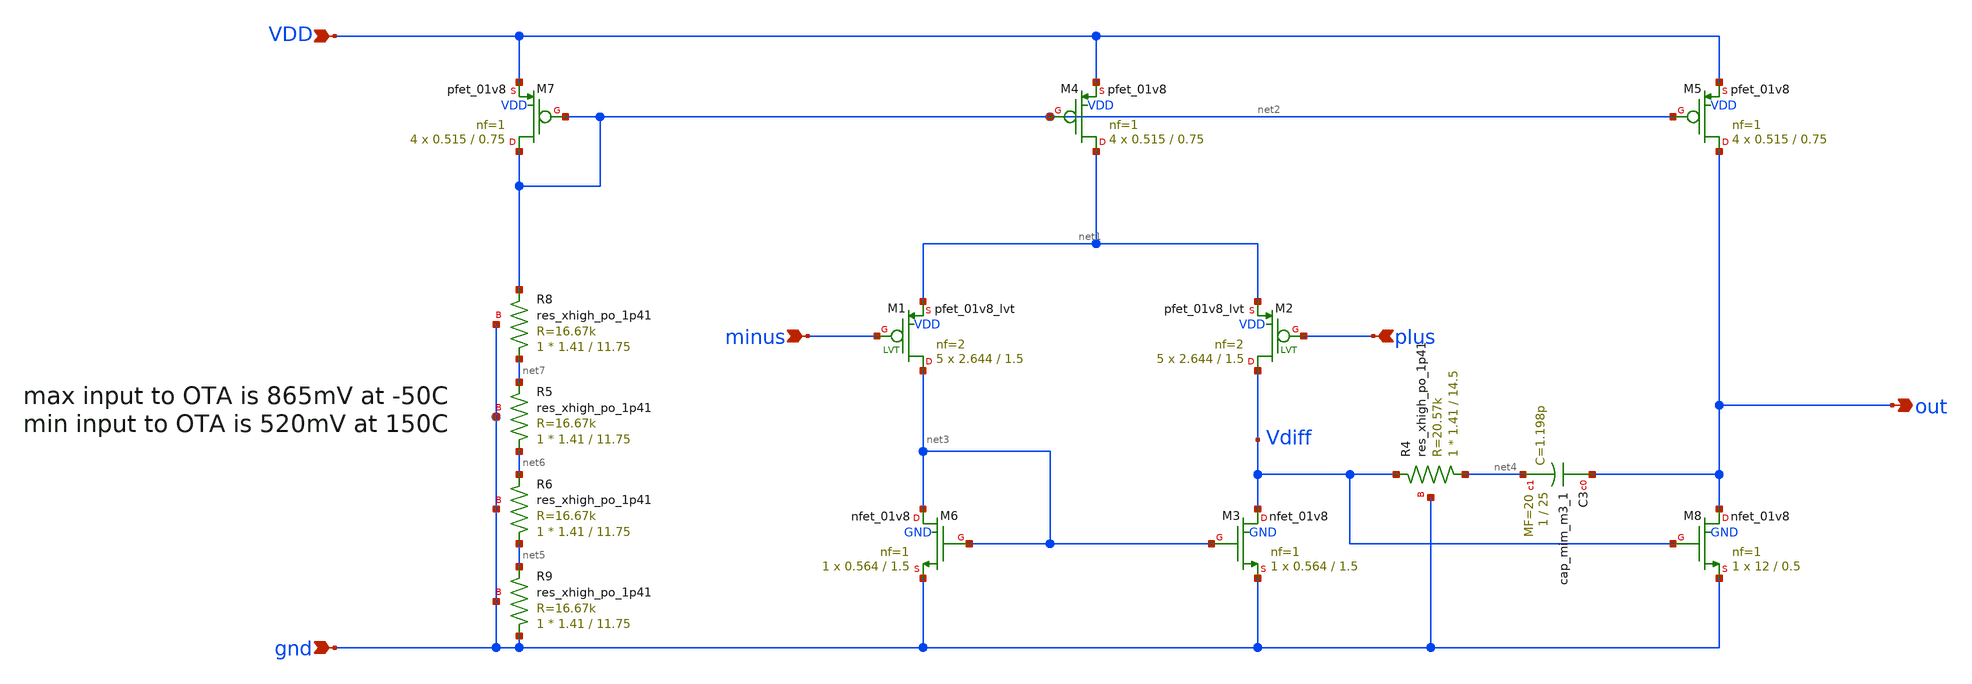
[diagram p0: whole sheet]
** sch_path: sky130_tests/ota1tb.sch
**.subckt ota1tb minus plus VDD gnd out
*.ipin minus
*.ipin plus
*.ipin VDD
*.ipin gnd
*.opin out
XM6 net3 net3 gnd GND sky130_fd_pr__nfet_01v8 L=1.5 W=0.564 nf=1 ad='int((1 + 1)/2) * 0.564 / 1 * 0.29'
+ as='int((1 + 2)/2) * 0.564 / 1 * 0.29' pd='2*int((1 + 1)/2) * (0.564 / 1 + 0.29)' ps='2*int((1 + 2)/2) * (0.564 / 1 + 0.29)'
+ nrd='0.29 / 0.564 ' nrs='0.29 / 0.564 ' sa=0 sb=0 sd=0 mult=1 m=1
XM8 out Vdiff gnd GND sky130_fd_pr__nfet_01v8 L=0.5 W=12 nf=1 ad='int((1 + 1)/2) * 12 / 1 * 0.29' as='int((1 + 2)/2) * 12 / 1 * 0.29'
+ pd='2*int((1 + 1)/2) * (12 / 1 + 0.29)' ps='2*int((1 + 2)/2) * (12 / 1 + 0.29)' nrd='0.29 / 12 ' nrs='0.29 / 12 '
+ sa=0 sb=0 sd=0 mult=1 m=1
XM1 net3 minus net1 VDD sky130_fd_pr__pfet_01v8_lvt L=1.5 W=2.644 nf=2 ad='int((2 + 1)/2) * 2.644 / 2 * 0.29'
+ as='int((2 + 2)/2) * 2.644 / 2 * 0.29' pd='2*int((2 + 1)/2) * (2.644 / 2 + 0.29)' ps='2*int((2 + 2)/2) * (2.644 / 2 + 0.29)'
+ nrd='0.29 / 2.644 ' nrs='0.29 / 2.644 ' sa=0 sb=0 sd=0 mult=5 m=5
XM3 Vdiff net3 gnd GND sky130_fd_pr__nfet_01v8 L=1.5 W=0.564 nf=1 ad='int((1 + 1)/2) * 0.564 / 1 * 0.29'
+ as='int((1 + 2)/2) * 0.564 / 1 * 0.29' pd='2*int((1 + 1)/2) * (0.564 / 1 + 0.29)' ps='2*int((1 + 2)/2) * (0.564 / 1 + 0.29)'
+ nrd='0.29 / 0.564 ' nrs='0.29 / 0.564 ' sa=0 sb=0 sd=0 mult=1 m=1
XM4 net1 net2 VDD VDD sky130_fd_pr__pfet_01v8 L=0.75 W=0.515 nf=1 ad='int((1 + 1)/2) * 0.515 / 1 * 0.29'
+ as='int((1 + 2)/2) * 0.515 / 1 * 0.29' pd='2*int((1 + 1)/2) * (0.515 / 1 + 0.29)' ps='2*int((1 + 2)/2) * (0.515 / 1 + 0.29)'
+ nrd='0.29 / 0.515 ' nrs='0.29 / 0.515 ' sa=0 sb=0 sd=0 mult=4 m=4
XM2 Vdiff plus net1 VDD sky130_fd_pr__pfet_01v8_lvt L=1.5 W=2.644 nf=2 ad='int((2 + 1)/2) * 2.644 / 2 * 0.29'
+ as='int((2 + 2)/2) * 2.644 / 2 * 0.29' pd='2*int((2 + 1)/2) * (2.644 / 2 + 0.29)' ps='2*int((2 + 2)/2) * (2.644 / 2 + 0.29)'
+ nrd='0.29 / 2.644 ' nrs='0.29 / 2.644 ' sa=0 sb=0 sd=0 mult=5 m=5
XR4 net4 Vdiff gnd sky130_fd_pr__res_xhigh_po_1p41 L=14.5 mult=1 m=1
XC3 out net4 sky130_fd_pr__cap_mim_m3_1 W=1 L=25 MF=20 m=20
XM7 net2 net2 VDD VDD sky130_fd_pr__pfet_01v8 L=0.75 W=0.515 nf=1 ad='int((1 + 1)/2) * 0.515 / 1 * 0.29'
+ as='int((1 + 2)/2) * 0.515 / 1 * 0.29' pd='2*int((1 + 1)/2) * (0.515 / 1 + 0.29)' ps='2*int((1 + 2)/2) * (0.515 / 1 + 0.29)'
+ nrd='0.29 / 0.515 ' nrs='0.29 / 0.515 ' sa=0 sb=0 sd=0 mult=4 m=4
XM5 out net2 VDD VDD sky130_fd_pr__pfet_01v8 L=0.75 W=0.515 nf=1 ad='int((1 + 1)/2) * 0.515 / 1 * 0.29'
+ as='int((1 + 2)/2) * 0.515 / 1 * 0.29' pd='2*int((1 + 1)/2) * (0.515 / 1 + 0.29)' ps='2*int((1 + 2)/2) * (0.515 / 1 + 0.29)'
+ nrd='0.29 / 0.515 ' nrs='0.29 / 0.515 ' sa=0 sb=0 sd=0 mult=4 m=4
XR8 net7 net2 gnd sky130_fd_pr__res_xhigh_po_1p41 L=11.75 mult=1 m=1
XR5 net6 net7 gnd sky130_fd_pr__res_xhigh_po_1p41 L=11.75 mult=1 m=1
XR6 net5 net6 gnd sky130_fd_pr__res_xhigh_po_1p41 L=11.75 mult=1 m=1
XR9 gnd net5 gnd sky130_fd_pr__res_xhigh_po_1p41 L=11.75 mult=1 m=1
**.ends
.end
